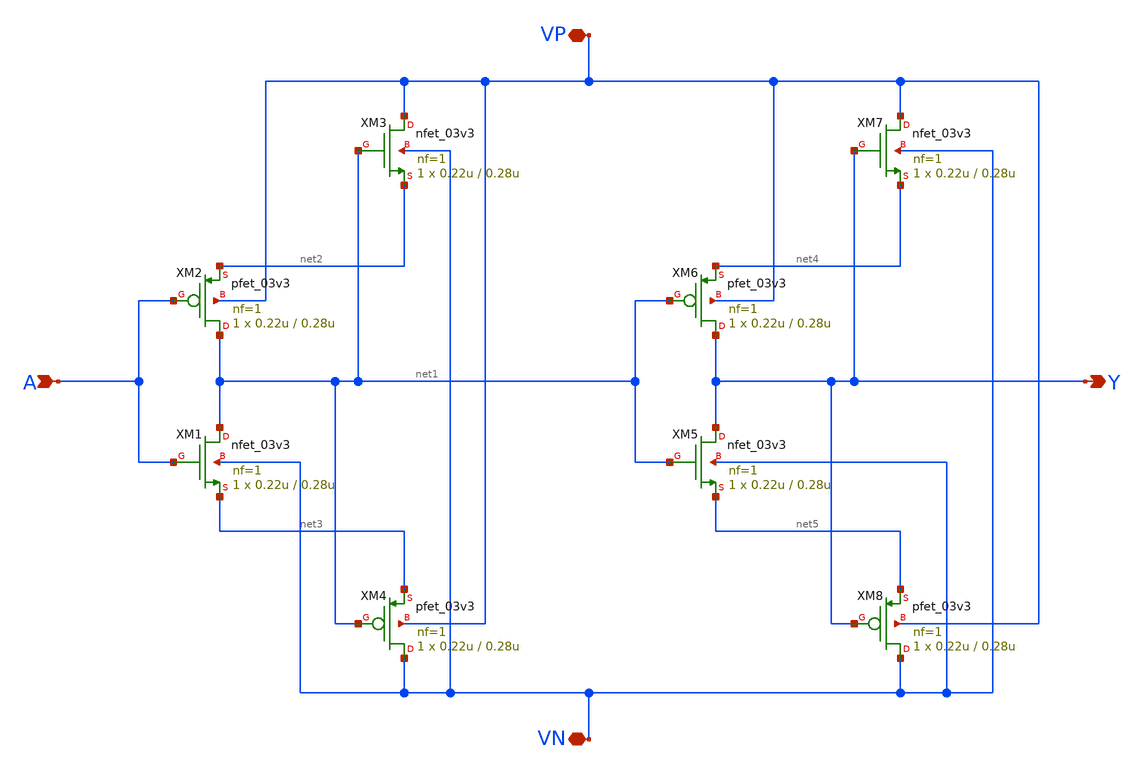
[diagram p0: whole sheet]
** sch_path: dls_buffer.sch
**.subckt dls_buffer A VN VP Y
*.ipin A
*.iopin VN
*.iopin VP
*.opin Y
XM1 net1 A net3 VN nfet_03v3 L=0.28u W=0.22u nf=1 ad='int((nf+1)/2) * W/nf * 0.18u' as='int((nf+2)/2) * W/nf * 0.18u'
+ pd='2*int((nf+1)/2) * (W/nf + 0.18u)' ps='2*int((nf+2)/2) * (W/nf + 0.18u)' nrd='0.18u / W' nrs='0.18u / W'
+ sa=0 sb=0 sd=0 m=1 par=1
XM2 net1 A net2 VP pfet_03v3 L=0.28u W=0.22u nf=1 ad='int((nf+1)/2) * W/nf * 0.18u' as='int((nf+2)/2) * W/nf * 0.18u'
+ pd='2*int((nf+1)/2) * (W/nf + 0.18u)' ps='2*int((nf+2)/2) * (W/nf + 0.18u)' nrd='0.18u / W' nrs='0.18u / W'
+ sa=0 sb=0 sd=0 m=1 par=1
XM3 VP net1 net2 VN nfet_03v3 L=0.28u W=0.22u nf=1 ad='int((nf+1)/2) * W/nf * 0.18u' as='int((nf+2)/2) * W/nf * 0.18u'
+ pd='2*int((nf+1)/2) * (W/nf + 0.18u)' ps='2*int((nf+2)/2) * (W/nf + 0.18u)' nrd='0.18u / W' nrs='0.18u / W'
+ sa=0 sb=0 sd=0 m=1 par=1
XM4 VN net1 net3 VP pfet_03v3 L=0.28u W=0.22u nf=1 ad='int((nf+1)/2) * W/nf * 0.18u' as='int((nf+2)/2) * W/nf * 0.18u'
+ pd='2*int((nf+1)/2) * (W/nf + 0.18u)' ps='2*int((nf+2)/2) * (W/nf + 0.18u)' nrd='0.18u / W' nrs='0.18u / W'
+ sa=0 sb=0 sd=0 m=1 par=1
XM5 Y net1 net5 VN nfet_03v3 L=0.28u W=0.22u nf=1 ad='int((nf+1)/2) * W/nf * 0.18u' as='int((nf+2)/2) * W/nf * 0.18u'
+ pd='2*int((nf+1)/2) * (W/nf + 0.18u)' ps='2*int((nf+2)/2) * (W/nf + 0.18u)' nrd='0.18u / W' nrs='0.18u / W'
+ sa=0 sb=0 sd=0 m=1 par=1
XM6 Y net1 net4 VP pfet_03v3 L=0.28u W=0.22u nf=1 ad='int((nf+1)/2) * W/nf * 0.18u' as='int((nf+2)/2) * W/nf * 0.18u'
+ pd='2*int((nf+1)/2) * (W/nf + 0.18u)' ps='2*int((nf+2)/2) * (W/nf + 0.18u)' nrd='0.18u / W' nrs='0.18u / W'
+ sa=0 sb=0 sd=0 m=1 par=1
XM7 VP Y net4 VN nfet_03v3 L=0.28u W=0.22u nf=1 ad='int((nf+1)/2) * W/nf * 0.18u' as='int((nf+2)/2) * W/nf * 0.18u'
+ pd='2*int((nf+1)/2) * (W/nf + 0.18u)' ps='2*int((nf+2)/2) * (W/nf + 0.18u)' nrd='0.18u / W' nrs='0.18u / W'
+ sa=0 sb=0 sd=0 m=1 par=1
XM8 VN Y net5 VP pfet_03v3 L=0.28u W=0.22u nf=1 ad='int((nf+1)/2) * W/nf * 0.18u' as='int((nf+2)/2) * W/nf * 0.18u'
+ pd='2*int((nf+1)/2) * (W/nf + 0.18u)' ps='2*int((nf+2)/2) * (W/nf + 0.18u)' nrd='0.18u / W' nrs='0.18u / W'
+ sa=0 sb=0 sd=0 m=1 par=1
**.ends
.end
